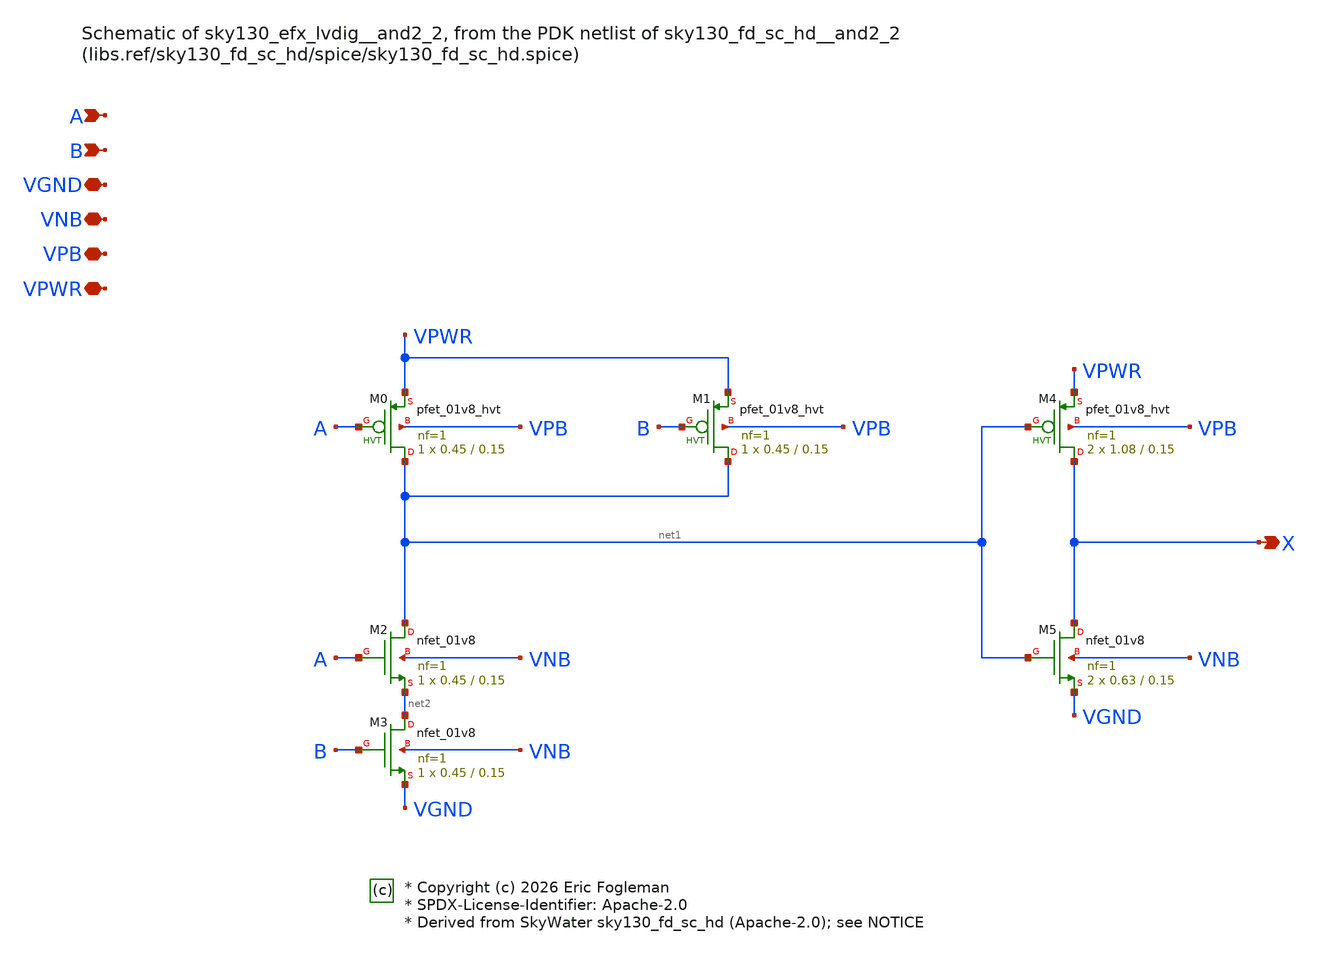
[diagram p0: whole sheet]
** sch_path: xschem/sky130_efx_lvdig__and2_2.sch

* Copyright (c) 2026 Eric Fogleman
* SPDX-License-Identifier: Apache-2.0
* Derived from SkyWater sky130_fd_sc_hd (Apache-2.0); see NOTICE

**.subckt sky130_efx_lvdig__and2_2 X A B VGND VNB VPB VPWR
*.opin X
*.ipin A
*.ipin B
*.iopin VGND
*.iopin VNB
*.iopin VPB
*.iopin VPWR
XM0 net1 A VPWR VPB sky130_fd_pr__pfet_01v8_hvt L=0.15 W=0.45 nf=1 ad='int((1 + 1)/2) * 0.45 / 1 * 0.29'
+ as='int((1 + 2)/2) * 0.45 / 1 * 0.29' pd='2*int((1 + 1)/2) * (0.45 / 1 + 0.29)' ps='2*int((1 + 2)/2) * (0.45 / 1 + 0.29)'
+ nrd='0.29 / 0.45 ' nrs='0.29 / 0.45 ' sa=0 sb=0 sd=0 mult=1 m=1
XM1 net1 B VPWR VPB sky130_fd_pr__pfet_01v8_hvt L=0.15 W=0.45 nf=1 ad='int((1 + 1)/2) * 0.45 / 1 * 0.29'
+ as='int((1 + 2)/2) * 0.45 / 1 * 0.29' pd='2*int((1 + 1)/2) * (0.45 / 1 + 0.29)' ps='2*int((1 + 2)/2) * (0.45 / 1 + 0.29)'
+ nrd='0.29 / 0.45 ' nrs='0.29 / 0.45 ' sa=0 sb=0 sd=0 mult=1 m=1
XM2 net1 A net2 VNB sky130_fd_pr__nfet_01v8 L=0.15 W=0.45 nf=1 ad='int((1 + 1)/2) * 0.45 / 1 * 0.29'
+ as='int((1 + 2)/2) * 0.45 / 1 * 0.29' pd='2*int((1 + 1)/2) * (0.45 / 1 + 0.29)' ps='2*int((1 + 2)/2) * (0.45 / 1 + 0.29)'
+ nrd='0.29 / 0.45 ' nrs='0.29 / 0.45 ' sa=0 sb=0 sd=0 mult=1 m=1
XM3 net2 B VGND VNB sky130_fd_pr__nfet_01v8 L=0.15 W=0.45 nf=1 ad='int((1 + 1)/2) * 0.45 / 1 * 0.29'
+ as='int((1 + 2)/2) * 0.45 / 1 * 0.29' pd='2*int((1 + 1)/2) * (0.45 / 1 + 0.29)' ps='2*int((1 + 2)/2) * (0.45 / 1 + 0.29)'
+ nrd='0.29 / 0.45 ' nrs='0.29 / 0.45 ' sa=0 sb=0 sd=0 mult=1 m=1
XM4 X net1 VPWR VPB sky130_fd_pr__pfet_01v8_hvt L=0.15 W=1.08 nf=1 ad='int((1 + 1)/2) * 1.08 / 1 * 0.29'
+ as='int((1 + 2)/2) * 1.08 / 1 * 0.29' pd='2*int((1 + 1)/2) * (1.08 / 1 + 0.29)' ps='2*int((1 + 2)/2) * (1.08 / 1 + 0.29)'
+ nrd='0.29 / 1.08 ' nrs='0.29 / 1.08 ' sa=0 sb=0 sd=0 mult=2 m=2
XM5 X net1 VGND VNB sky130_fd_pr__nfet_01v8 L=0.15 W=0.63 nf=1 ad='int((1 + 1)/2) * 0.63 / 1 * 0.29'
+ as='int((1 + 2)/2) * 0.63 / 1 * 0.29' pd='2*int((1 + 1)/2) * (0.63 / 1 + 0.29)' ps='2*int((1 + 2)/2) * (0.63 / 1 + 0.29)'
+ nrd='0.29 / 0.63 ' nrs='0.29 / 0.63 ' sa=0 sb=0 sd=0 mult=2 m=2
**.ends
.end
